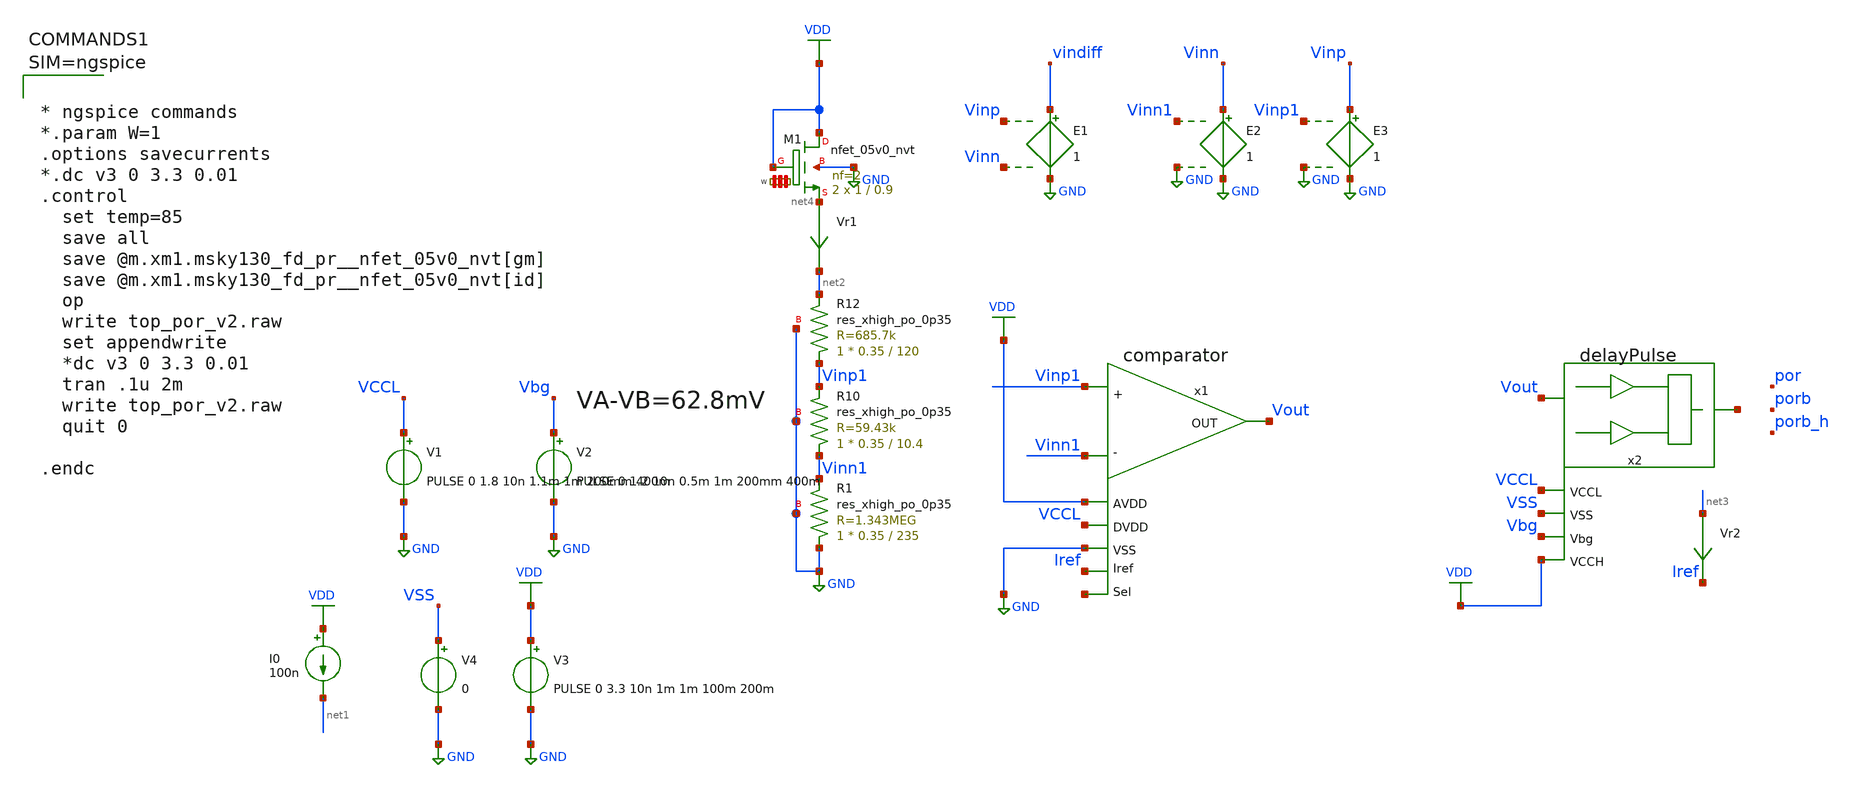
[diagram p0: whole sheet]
** sch_path: xschem/top_por_v2.sch
**.subckt top_por_v2
V3 VDD GND PULSE 0 3.3 10n 1m 1m 100m 200m
I0 VDD net1 100n
XM1 VDD VDD net4 GND sky130_fd_pr__nfet_05v0_nvt L=0.9 W='1 * 2 ' nf=2 ad='int((nf+1)/2) * W / nf * 0.29'
+ as='int((nf+2)/2) * W / nf * 0.29' pd='2*int((nf+1)/2) * (W / nf + 0.29)' ps='2*int((nf+2)/2) * (W / nf + 0.29)'
+ nrd='0.29 / W ' nrs='0.29 / W ' sa=0 sb=0 sd=0 mult=2 m=2
Vr1 net4 net2 0
.save i(vr1)
E1 vindiff GND Vinp Vinn 1
x1 Iref Vinn1 Vinp1 Vout GND VDD VCCL net5 comparator
XR1 GND Vinn1 GND sky130_fd_pr__res_xhigh_po_0p35 L=235 mult=1 m=1
XR10 Vinn1 Vinp1 GND sky130_fd_pr__res_xhigh_po_0p35 L=10.4 mult=1 m=1
XR12 Vinp1 net2 GND sky130_fd_pr__res_xhigh_po_0p35 L=120 mult=1 m=1
x2 Vout net6 VCCL VSS Vbg VDD delayPulse
V1 VCCL GND PULSE 0 1.8 10n 1.1m 1m 200mm 400m
V2 Vbg GND PULSE 0 1.2 10n 0.5m 1m 200mm 400m
V4 VSS GND 0
E2 Vinn GND Vinn1 GND 1
E3 Vinp GND Vinp1 GND 1
Vr2 net3 Iref 0
.save i(vr2)
**** begin user architecture code



* ngspice commands
*.param W=1
.options savecurrents
*.dc v3 0 3.3 0.01
.control
  set temp=85
  save all
  save @m.xm1.msky130_fd_pr__nfet_05v0_nvt[gm]
  save @m.xm1.msky130_fd_pr__nfet_05v0_nvt[id]
  op
  write top_por_v2.raw
  set appendwrite
  *dc v3 0 3.3 0.01
  tran .1u 2m
  write top_por_v2.raw
  quit 0

.endc



 .lib $::SKYWATER_MODELS/sky130.lib.spice tt

.include $::SKYWATER_STDCELLS/sky130_fd_sc_hd.spice
.include /foss/pdks/sky130A/libs.ref/sky130_fd_sc_hvl/spice/sky130_fd_sc_hvl.spice


**** end user architecture code
**.ends
.GLOBAL GND
.GLOBAL VDD
.end
